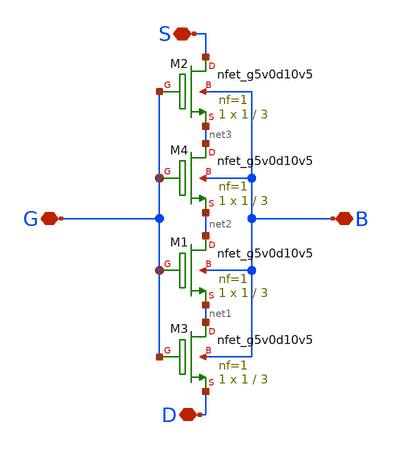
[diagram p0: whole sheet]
** sch_path: xschem/n_4_s_1_3.sch
**.subckt n_4_s_1_3 S D B G
*.iopin S
*.iopin D
*.iopin B
*.iopin G
XM1 net2 G net1 B sky130_fd_pr__nfet_g5v0d10v5 L=3 W=1 nf=1 ad='int((nf+1)/2) * W/nf * 0.29' as='int((nf+2)/2) * W/nf * 0.29'
+ pd='2*int((nf+1)/2) * (W/nf + 0.29)' ps='2*int((nf+2)/2) * (W/nf + 0.29)' nrd='0.29 / W' nrs='0.29 / W'
+ sa=0 sb=0 sd=0 mult=1 m=1
XM2 S G net3 B sky130_fd_pr__nfet_g5v0d10v5 L=3 W=1 nf=1 ad='int((nf+1)/2) * W/nf * 0.29' as='int((nf+2)/2) * W/nf * 0.29'
+ pd='2*int((nf+1)/2) * (W/nf + 0.29)' ps='2*int((nf+2)/2) * (W/nf + 0.29)' nrd='0.29 / W' nrs='0.29 / W'
+ sa=0 sb=0 sd=0 mult=1 m=1
XM3 net1 G D B sky130_fd_pr__nfet_g5v0d10v5 L=3 W=1 nf=1 ad='int((nf+1)/2) * W/nf * 0.29' as='int((nf+2)/2) * W/nf * 0.29'
+ pd='2*int((nf+1)/2) * (W/nf + 0.29)' ps='2*int((nf+2)/2) * (W/nf + 0.29)' nrd='0.29 / W' nrs='0.29 / W'
+ sa=0 sb=0 sd=0 mult=1 m=1
XM4 net3 G net2 B sky130_fd_pr__nfet_g5v0d10v5 L=3 W=1 nf=1 ad='int((nf+1)/2) * W/nf * 0.29' as='int((nf+2)/2) * W/nf * 0.29'
+ pd='2*int((nf+1)/2) * (W/nf + 0.29)' ps='2*int((nf+2)/2) * (W/nf + 0.29)' nrd='0.29 / W' nrs='0.29 / W'
+ sa=0 sb=0 sd=0 mult=1 m=1
**.ends
.end
